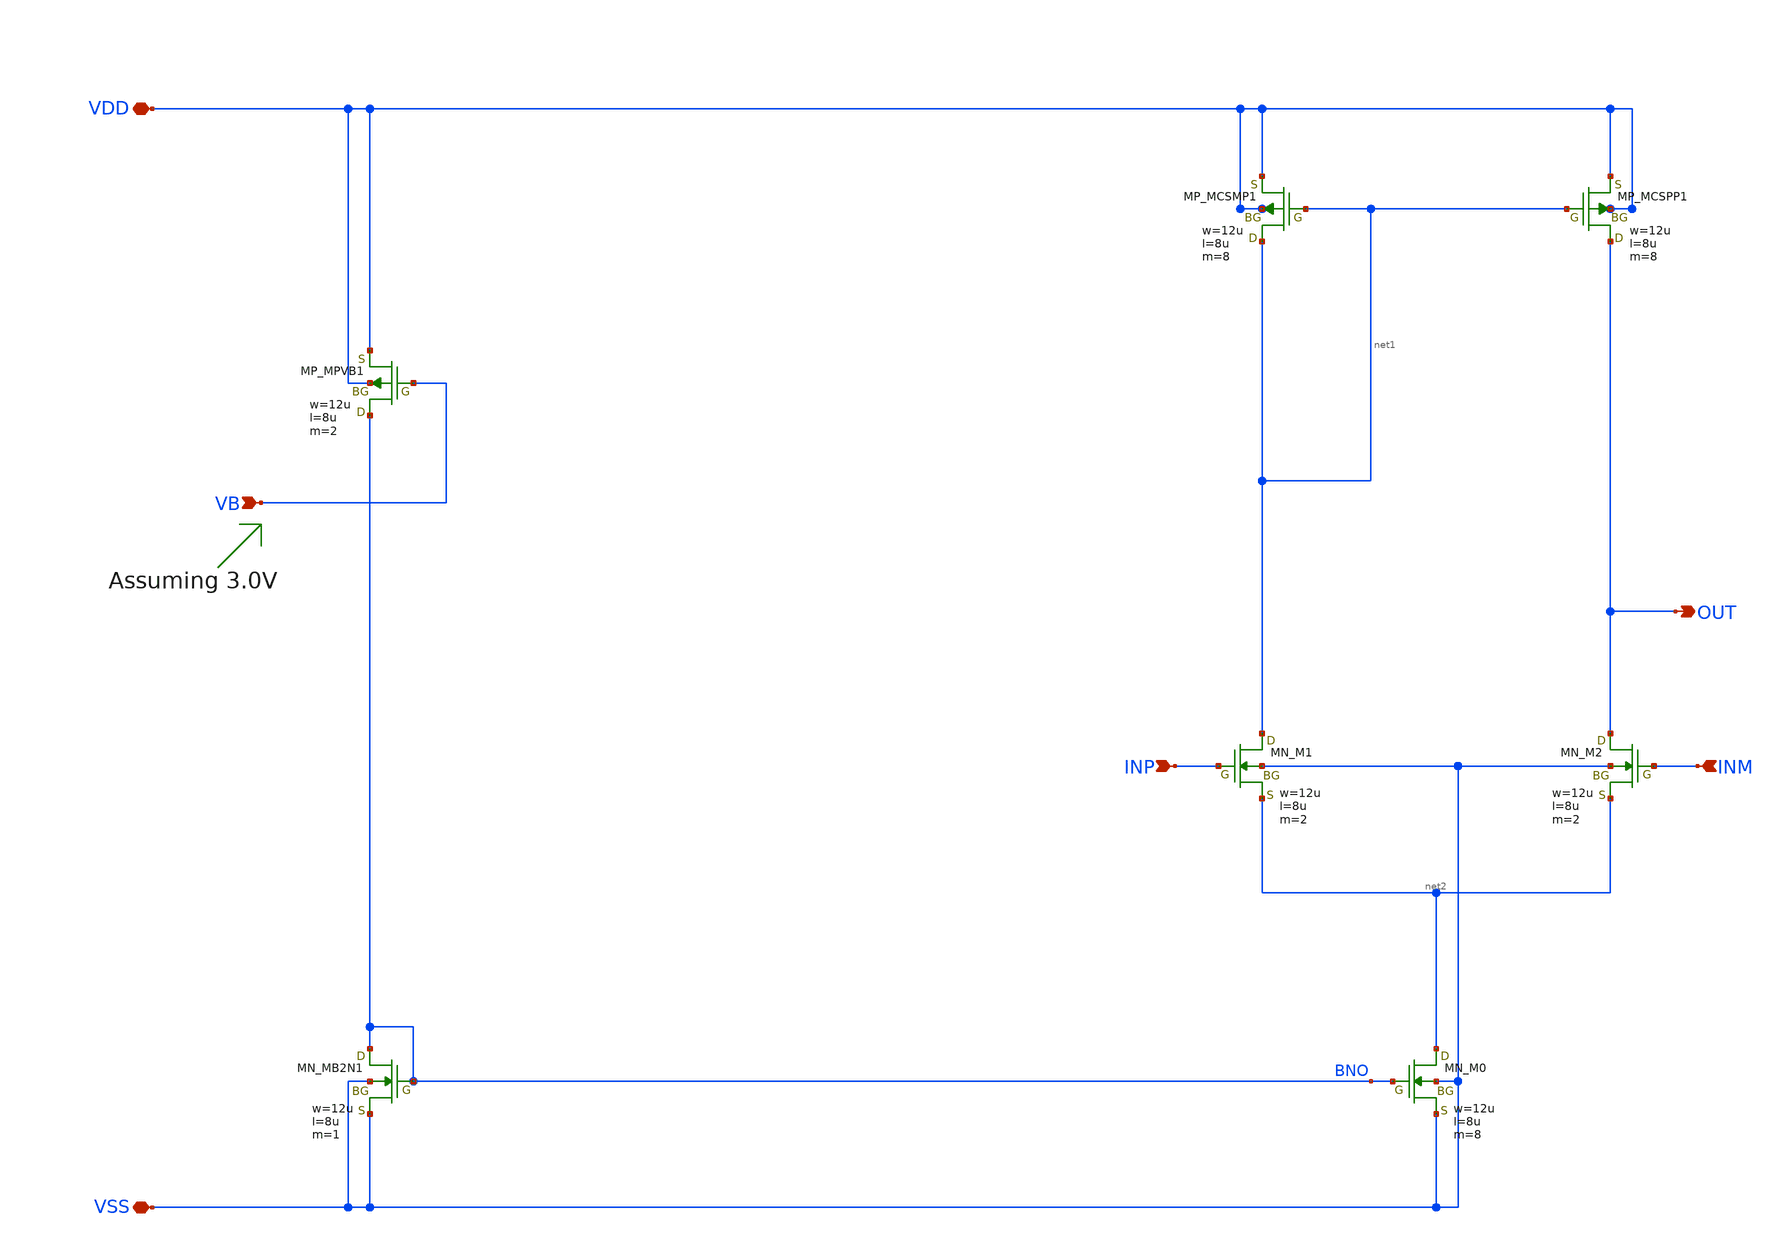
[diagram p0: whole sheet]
** sch_path: OpenSUSI-TR10/opamp_r2r/ota_noccm_1st.sch
**.subckt ota_noccm_1st VDD VSS INP INM VB OUT
*.iopin VDD
*.iopin VSS
*.ipin INP
*.ipin INM
*.ipin VB
*.opin OUT
XMB2N1 BNO BNO VSS VSS NMOS w=12u l=8u as=0 ad=0 ps=0 pd=0 nrd=0 nrs=0 m=1
XM0 net2 BNO VSS VSS NMOS w=12u l=8u as=0 ad=0 ps=0 pd=0 nrd=0 nrs=0 m=8
XM1 net1 INP net2 VSS NMOS w=12u l=8u as=0 ad=0 ps=0 pd=0 nrd=0 nrs=0 m=2
XM2 OUT INM net2 VSS NMOS w=12u l=8u as=0 ad=0 ps=0 pd=0 nrd=0 nrs=0 m=2
XMCSMP1 net1 net1 VDD VDD PMOS w=12u l=8u as=0 ad=0 ps=0 pd=0 nrd=0 nrs=0 m=8
XMCSPP1 OUT net1 VDD VDD PMOS w=12u l=8u as=0 ad=0 ps=0 pd=0 nrd=0 nrs=0 m=8
XMPVB1 BNO VB VDD VDD PMOS w=12u l=8u as=0 ad=0 ps=0 pd=0 nrd=0 nrs=0 m=2
**.ends
.end
